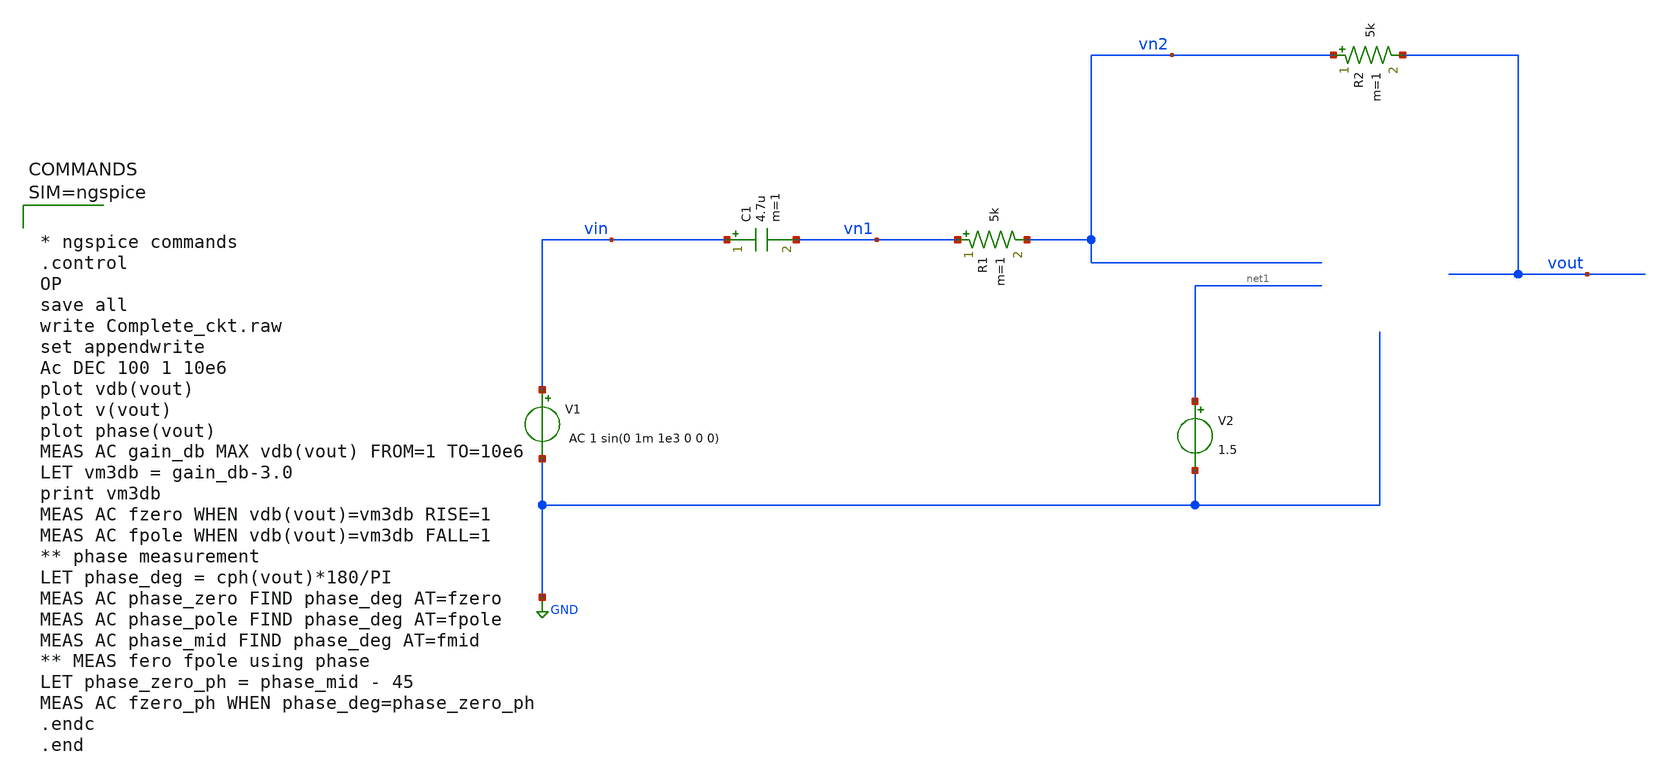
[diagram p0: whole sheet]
** sch_path: xschem/oplowpass.sch
**.subckt oplowpass
R1 vn1 vn2 5k m=1
R2 vn2 vout 5k m=1
C1 vin vn1 4.7u m=1
V1 vin GND AC 1 sin(0 1m 1e3 0 0 0)
V2 net1 GND 1.5
**** begin user architecture code



* ngspice commands
.control
OP
save all
write Complete_ckt.raw
set appendwrite
Ac DEC 100 1 10e6
plot vdb(vout)
plot v(vout)
plot phase(vout)
MEAS AC gain_db MAX vdb(vout) FROM=1 TO=10e6
LET vm3db = gain_db-3.0
print vm3db
MEAS AC fzero WHEN vdb(vout)=vm3db RISE=1
MEAS AC fpole WHEN vdb(vout)=vm3db FALL=1
** phase measurement
LET phase_deg = cph(vout)*180/PI
MEAS AC phase_zero FIND phase_deg AT=fzero
MEAS AC phase_pole FIND phase_deg AT=fpole
MEAS AC phase_mid FIND phase_deg AT=fmid
** MEAS fero fpole using phase
LET phase_zero_ph = phase_mid - 45
MEAS AC fzero_ph WHEN phase_deg=phase_zero_ph
.endc
.end



**** end user architecture code
**.ends
.GLOBAL GND
.end
